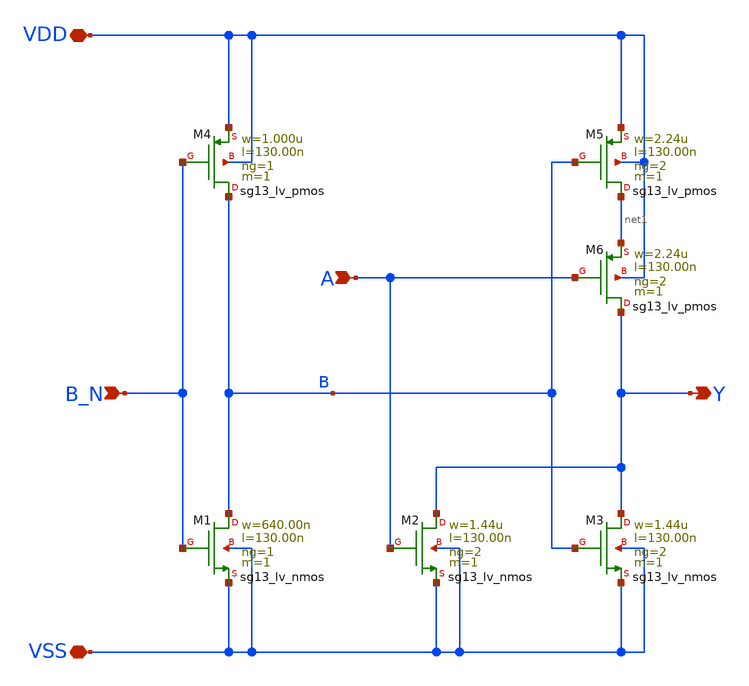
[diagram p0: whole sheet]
** sch_path: ihp-sg13g2/libs.tech/xschem/sg13g2_stdcells/sg13g2_nor2b_2.sch
* Copyright 2023 IHP PDK Authors
* Licensed under the Apache License, Version 2.0 (the "License");
* you may not use this file except in compliance with the License.
* You may obtain a copy of the License at
* https://www.apache.org/licenses/LICENSE-2.0
* Unless required by applicable law or agreed to in writing, software
* distributed under the License is distributed on an "AS IS" BASIS,
* WITHOUT WARRANTIES OR CONDITIONS OF ANY KIND, either express or implied.
* See the License for the specific language governing permissions and
* limitations under the License.
**.subckt sg13g2_nor2b_2 Y B_N A VDD VSS
*.opin Y
*.ipin B_N
*.ipin A
*.iopin VDD
*.iopin VSS
XM1 B B_N VSS VSS sg13_lv_nmos w=640.00n l=130.00n ng=1 m=1 mm_ok=1
XM2 Y A VSS VSS sg13_lv_nmos w=1.44u l=130.00n ng=2 m=1 mm_ok=1
XM3 Y B VSS VSS sg13_lv_nmos w=1.44u l=130.00n ng=2 m=1 mm_ok=1
XM4 B B_N VDD VDD sg13_lv_pmos w=1.000u l=130.00n ng=1 m=1 mm_ok=1
XM5 net1 B VDD VDD sg13_lv_pmos w=2.24u l=130.00n ng=2 m=1 mm_ok=1
XM6 Y A net1 VDD sg13_lv_pmos w=2.24u l=130.00n ng=2 m=1 mm_ok=1
**.ends
.end
